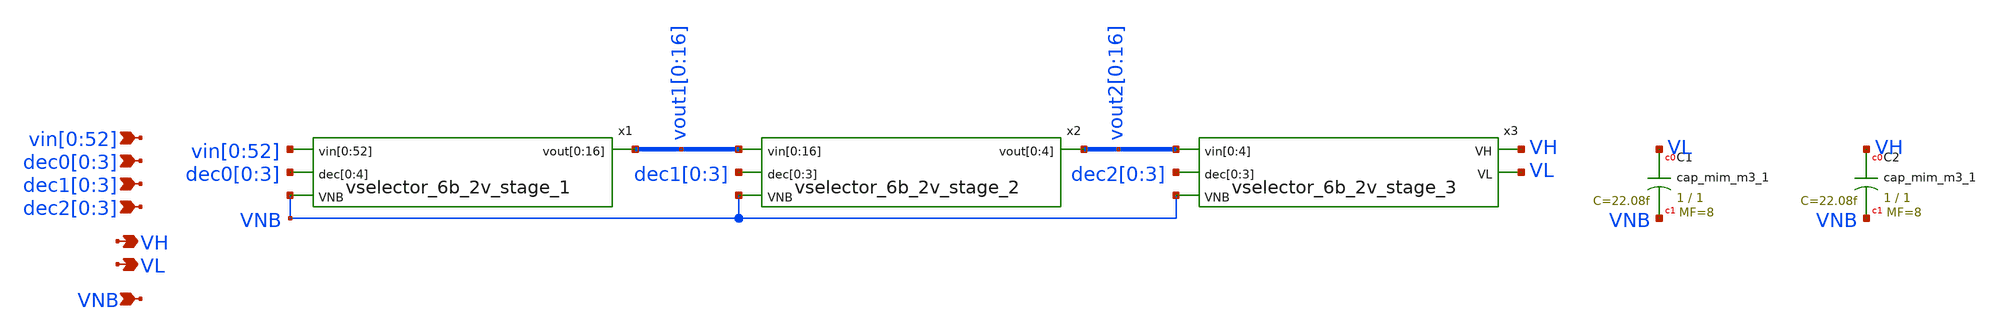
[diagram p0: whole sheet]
** sch_path: xschem/vselector_6b_2v.sch
**.subckt vselector_6b_2v
*+ vin[0],vin[1],vin[2],vin[3],vin[4],vin[5],vin[6],vin[7],vin[8],vin[9],vin[10],vin[11],vin[12],vin[13],vin[14],vin[15],vin[16],vin[17],vin[18],vin[19],vin[20],vin[21],vin[22],vin[23],vin[24],vin[25],vin[26],vin[27],vin[28],vin[29],vin[30],vin[31],vin[32],vin[33],vin[34],vin[35],vin[36],vin[37],vin[38],vin[39],vin[40],vin[41],vin[42],vin[43],vin[44],vin[45],vin[46],vin[47],vin[48],vin[49],vin[50],vin[51],vin[52] VH VNB dec0[0],dec0[1],dec0[2],dec0[3] VL dec1[0],dec1[1],dec1[2],dec1[3]
*+ dec2[0],dec2[1],dec2[2],dec2[3]
*.ipin
*+ vin[0],vin[1],vin[2],vin[3],vin[4],vin[5],vin[6],vin[7],vin[8],vin[9],vin[10],vin[11],vin[12],vin[13],vin[14],vin[15],vin[16],vin[17],vin[18],vin[19],vin[20],vin[21],vin[22],vin[23],vin[24],vin[25],vin[26],vin[27],vin[28],vin[29],vin[30],vin[31],vin[32],vin[33],vin[34],vin[35],vin[36],vin[37],vin[38],vin[39],vin[40],vin[41],vin[42],vin[43],vin[44],vin[45],vin[46],vin[47],vin[48],vin[49],vin[50],vin[51],vin[52]
*.opin VH
*.ipin VNB
*.ipin dec0[0],dec0[1],dec0[2],dec0[3]
*.opin VL
*.ipin dec1[0],dec1[1],dec1[2],dec1[3]
*.ipin dec2[0],dec2[1],dec2[2],dec2[3]
x1 vin[0] vin[1] vin[2] vin[3] vin[4] vin[5] vin[6] vin[7] vin[8] vin[9] vin[10] vin[11] vin[12]
+ vin[13] vin[14] vin[15] vin[16] vin[17] vin[18] vin[19] vin[20] vin[21] vin[22] vin[23] vin[24] vin[25]
+ vin[26] vin[27] vin[28] vin[29] vin[30] vin[31] vin[32] vin[33] vin[34] vin[35] vin[36] vin[37] vin[38]
+ vin[39] vin[40] vin[41] vin[42] vin[43] vin[44] vin[45] vin[46] vin[47] vin[48] vin[49] vin[50] vin[51]
+ vin[52] dec0[0] dec0[1] dec0[2] dec0[3] dec0[0] vout1[0] vout1[1] vout1[2] vout1[3] vout1[4] vout1[5]
+ vout1[6] vout1[7] vout1[8] vout1[9] vout1[10] vout1[11] vout1[12] vout1[13] vout1[14] vout1[15] vout1[16]
+ VNB vselector_6b_2v_stage_1
x2 vout1[0] vout1[1] vout1[2] vout1[3] vout1[4] vout1[5] vout1[6] vout1[7] vout1[8] vout1[9]
+ vout1[10] vout1[11] vout1[12] vout1[13] vout1[14] vout1[15] vout1[16] dec1[0] dec1[1] dec1[2] dec1[3]
+ vout2[0] vout2[1] vout2[2] vout2[3] vout2[4] VNB vselector_6b_2v_stage_2
x3 vout2[0] vout2[1] vout2[2] vout2[3] vout2[4] dec2[0] dec2[1] dec2[2] dec2[3] VH VL VNB
+ vselector_6b_2v_stage_3
XC1 VL VNB sky130_fd_pr__cap_mim_m3_1 W=1 L=1 MF=8 m=8
XC2 VH VNB sky130_fd_pr__cap_mim_m3_1 W=1 L=1 MF=8 m=8
**.ends

* expanding   symbol:  vselector_6b_2v_stage_1.sym # of pins=4
** sym_path: xschem/vselector_6b_2v_stage_1.sym
** sch_path: xschem/vselector_6b_2v_stage_1.sch
.subckt vselector_6b_2v_stage_1 vin[0] vin[1] vin[2] vin[3] vin[4] vin[5] vin[6] vin[7] vin[8]
+ vin[9] vin[10] vin[11] vin[12] vin[13] vin[14] vin[15] vin[16] vin[17] vin[18] vin[19] vin[20] vin[21]
+ vin[22] vin[23] vin[24] vin[25] vin[26] vin[27] vin[28] vin[29] vin[30] vin[31] vin[32] vin[33] vin[34]
+ vin[35] vin[36] vin[37] vin[38] vin[39] vin[40] vin[41] vin[42] vin[43] vin[44] vin[45] vin[46] vin[47]
+ vin[48] vin[49] vin[50] vin[51] vin[52] dec[0] dec[1] dec[2] dec[3] dec[4] vout[0] vout[1] vout[2] vout[3]
+ vout[4] vout[5] vout[6] vout[7] vout[8] vout[9] vout[10] vout[11] vout[12] vout[13] vout[14] vout[15]
+ vout[16] VNB
*.ipin
*+ vin[0],vin[1],vin[2],vin[3],vin[4],vin[5],vin[6],vin[7],vin[8],vin[9],vin[10],vin[11],vin[12],vin[13],vin[14],vin[15],vin[16],vin[17],vin[18],vin[19],vin[20],vin[21],vin[22],vin[23],vin[24],vin[25],vin[26],vin[27],vin[28],vin[29],vin[30],vin[31],vin[32],vin[33],vin[34],vin[35],vin[36],vin[37],vin[38],vin[39],vin[40],vin[41],vin[42],vin[43],vin[44],vin[45],vin[46],vin[47],vin[48],vin[49],vin[50],vin[51],vin[52]
*.opin
*+ vout[0],vout[1],vout[2],vout[3],vout[4],vout[5],vout[6],vout[7],vout[8],vout[9],vout[10],vout[11],vout[12],vout[13],vout[14],vout[15],vout[16]
*.ipin VNB
*.ipin dec[0],dec[1],dec[2],dec[3],dec[4]
x1 vin[0] vin[1] vin[2] vin[3] vin[4] vin[5] vin[6] vin[7] vin[8] vin[9] vin[10] vin[11] vin[12]
+ vin[13] vin[14] vin[15] vin[16] dec[0] vout[0] vout[1] vout[2] vout[3] vout[4] vout[5] vout[6] vout[7]
+ vout[8] vout[9] vout[10] vout[11] vout[12] vout[13] vout[14] vout[15] vout[16] VNB vselector_16b
x2 vin[16] vin[17] vin[18] vin[19] vin[20] vin[21] vin[22] vin[23] vin[24] vin[25] vin[26] vin[27]
+ vin[28] vin[29] vin[30] vin[31] vin[32] dec[1] vout[0] vout[1] vout[2] vout[3] vout[4] vout[5] vout[6]
+ vout[7] vout[8] vout[9] vout[10] vout[11] vout[12] vout[13] vout[14] vout[15] vout[16] VNB vselector_16b
x3 vin[32] vin[33] vin[34] vin[35] vin[36] vin[37] vin[38] vin[39] vin[40] vin[41] vin[42] vin[43]
+ vin[44] vin[45] vin[46] vin[47] vin[48] dec[2] vout[0] vout[1] vout[2] vout[3] vout[4] vout[5] vout[6]
+ vout[7] vout[8] vout[9] vout[10] vout[11] vout[12] vout[13] vout[14] vout[15] vout[16] VNB vselector_16b
x4 vin[48] vin[49] vin[50] vin[51] vin[52] dec[3] vout[0] vout[1] vout[2] vout[3] vout[4] VNB
+ vselector_4b
.ends


* expanding   symbol:  vselector_6b_2v_stage_2.sym # of pins=4
** sym_path: xschem/vselector_6b_2v_stage_2.sym
** sch_path: xschem/vselector_6b_2v_stage_2.sch
.subckt vselector_6b_2v_stage_2 vin[0] vin[1] vin[2] vin[3] vin[4] vin[5] vin[6] vin[7] vin[8]
+ vin[9] vin[10] vin[11] vin[12] vin[13] vin[14] vin[15] vin[16] dec[0] dec[1] dec[2] dec[3] vout[0] vout[1]
+ vout[2] vout[3] vout[4] VNB
*.ipin
*+ vin[0],vin[1],vin[2],vin[3],vin[4],vin[5],vin[6],vin[7],vin[8],vin[9],vin[10],vin[11],vin[12],vin[13],vin[14],vin[15],vin[16]
*.opin vout[0],vout[1],vout[2],vout[3],vout[4]
*.ipin VNB
*.ipin dec[0],dec[1],dec[2],dec[3]
x1 vin[0] vin[1] vin[2] vin[3] vin[4] dec[0] vout[0] vout[1] vout[2] vout[3] vout[4] VNB
+ vselector_4b
x2 vin[4] vin[5] vin[6] vin[7] vin[8] dec[1] vout[0] vout[1] vout[2] vout[3] vout[4] VNB
+ vselector_4b
x3 vin[8] vin[9] vin[10] vin[11] vin[12] dec[2] vout[0] vout[1] vout[2] vout[3] vout[4] VNB
+ vselector_4b
x4 vin[12] vin[13] vin[14] vin[15] vin[16] dec[3] vout[0] vout[1] vout[2] vout[3] vout[4] VNB
+ vselector_4b
.ends


* expanding   symbol:  vselector_6b_2v_stage_3.sym # of pins=5
** sym_path: xschem/vselector_6b_2v_stage_3.sym
** sch_path: xschem/vselector_6b_2v_stage_3.sch
.subckt vselector_6b_2v_stage_3 vin[0] vin[1] vin[2] vin[3] vin[4] dec[0] dec[1] dec[2] dec[3] VH VL
+ VNB
*.ipin vin[0],vin[1],vin[2],vin[3],vin[4]
*.opin VH
*.ipin VNB
*.ipin dec[0],dec[1],dec[2],dec[3]
*.opin VL
x1 vin[0] vin[1] dec[0] VH VL VNB vselector_1b
x2 vin[1] vin[2] dec[1] VH VL VNB vselector_1b
x3 vin[2] vin[3] dec[2] VH VL VNB vselector_1b
x4 vin[3] vin[4] dec[3] VH VL VNB vselector_1b
.ends


* expanding   symbol:  vselector_16b.sym # of pins=4
** sym_path: xschem/vselector_16b.sym
** sch_path: xschem/vselector_16b.sch
.subckt vselector_16b vin[0] vin[1] vin[2] vin[3] vin[4] vin[5] vin[6] vin[7] vin[8] vin[9] vin[10]
+ vin[11] vin[12] vin[13] vin[14] vin[15] vin[16] DIN vout[0] vout[1] vout[2] vout[3] vout[4] vout[5] vout[6]
+ vout[7] vout[8] vout[9] vout[10] vout[11] vout[12] vout[13] vout[14] vout[15] vout[16] VNB
*.ipin
*+ vin[0],vin[1],vin[2],vin[3],vin[4],vin[5],vin[6],vin[7],vin[8],vin[9],vin[10],vin[11],vin[12],vin[13],vin[14],vin[15],vin[16]
*.opin
*+ vout[0],vout[1],vout[2],vout[3],vout[4],vout[5],vout[6],vout[7],vout[8],vout[9],vout[10],vout[11],vout[12],vout[13],vout[14],vout[15],vout[16]
*.ipin VNB
*.ipin DIN
XM1 vout[0] DIN vin[0] VNB sky130_fd_pr__nfet_g5v0d10v5 L=l W=wn nf=1 ad='int((nf+1)/2) * W/nf * 0.29'
+ as='int((nf+2)/2) * W/nf * 0.29' pd='2*int((nf+1)/2) * (W/nf + 0.29)' ps='2*int((nf+2)/2) * (W/nf + 0.29)'
+ nrd='0.29 / W' nrs='0.29 / W' sa=0 sb=0 sd=0 mult=1 m=1
XM2 vout[1] DIN vin[1] VNB sky130_fd_pr__nfet_g5v0d10v5 L=l W=wn nf=1 ad='int((nf+1)/2) * W/nf * 0.29'
+ as='int((nf+2)/2) * W/nf * 0.29' pd='2*int((nf+1)/2) * (W/nf + 0.29)' ps='2*int((nf+2)/2) * (W/nf + 0.29)'
+ nrd='0.29 / W' nrs='0.29 / W' sa=0 sb=0 sd=0 mult=1 m=1
XM3 vout[2] DIN vin[2] VNB sky130_fd_pr__nfet_g5v0d10v5 L=l W=wn nf=1 ad='int((nf+1)/2) * W/nf * 0.29'
+ as='int((nf+2)/2) * W/nf * 0.29' pd='2*int((nf+1)/2) * (W/nf + 0.29)' ps='2*int((nf+2)/2) * (W/nf + 0.29)'
+ nrd='0.29 / W' nrs='0.29 / W' sa=0 sb=0 sd=0 mult=1 m=1
XM4 vout[3] DIN vin[3] VNB sky130_fd_pr__nfet_g5v0d10v5 L=l W=wn nf=1 ad='int((nf+1)/2) * W/nf * 0.29'
+ as='int((nf+2)/2) * W/nf * 0.29' pd='2*int((nf+1)/2) * (W/nf + 0.29)' ps='2*int((nf+2)/2) * (W/nf + 0.29)'
+ nrd='0.29 / W' nrs='0.29 / W' sa=0 sb=0 sd=0 mult=1 m=1
XM5 vout[4] DIN vin[4] VNB sky130_fd_pr__nfet_g5v0d10v5 L=l W=wn nf=1 ad='int((nf+1)/2) * W/nf * 0.29'
+ as='int((nf+2)/2) * W/nf * 0.29' pd='2*int((nf+1)/2) * (W/nf + 0.29)' ps='2*int((nf+2)/2) * (W/nf + 0.29)'
+ nrd='0.29 / W' nrs='0.29 / W' sa=0 sb=0 sd=0 mult=1 m=1
XM6 vout[5] DIN vin[5] VNB sky130_fd_pr__nfet_g5v0d10v5 L=l W=wn nf=1 ad='int((nf+1)/2) * W/nf * 0.29'
+ as='int((nf+2)/2) * W/nf * 0.29' pd='2*int((nf+1)/2) * (W/nf + 0.29)' ps='2*int((nf+2)/2) * (W/nf + 0.29)'
+ nrd='0.29 / W' nrs='0.29 / W' sa=0 sb=0 sd=0 mult=1 m=1
XM7 vout[6] DIN vin[6] VNB sky130_fd_pr__nfet_g5v0d10v5 L=l W=wn nf=1 ad='int((nf+1)/2) * W/nf * 0.29'
+ as='int((nf+2)/2) * W/nf * 0.29' pd='2*int((nf+1)/2) * (W/nf + 0.29)' ps='2*int((nf+2)/2) * (W/nf + 0.29)'
+ nrd='0.29 / W' nrs='0.29 / W' sa=0 sb=0 sd=0 mult=1 m=1
XM8 vout[7] DIN vin[7] VNB sky130_fd_pr__nfet_g5v0d10v5 L=l W=wn nf=1 ad='int((nf+1)/2) * W/nf * 0.29'
+ as='int((nf+2)/2) * W/nf * 0.29' pd='2*int((nf+1)/2) * (W/nf + 0.29)' ps='2*int((nf+2)/2) * (W/nf + 0.29)'
+ nrd='0.29 / W' nrs='0.29 / W' sa=0 sb=0 sd=0 mult=1 m=1
XM9 vout[8] DIN vin[8] VNB sky130_fd_pr__nfet_g5v0d10v5 L=l W=wn nf=1 ad='int((nf+1)/2) * W/nf * 0.29'
+ as='int((nf+2)/2) * W/nf * 0.29' pd='2*int((nf+1)/2) * (W/nf + 0.29)' ps='2*int((nf+2)/2) * (W/nf + 0.29)'
+ nrd='0.29 / W' nrs='0.29 / W' sa=0 sb=0 sd=0 mult=1 m=1
XM10 vout[9] DIN vin[9] VNB sky130_fd_pr__nfet_g5v0d10v5 L=l W=wn nf=1 ad='int((nf+1)/2) * W/nf * 0.29'
+ as='int((nf+2)/2) * W/nf * 0.29' pd='2*int((nf+1)/2) * (W/nf + 0.29)' ps='2*int((nf+2)/2) * (W/nf + 0.29)'
+ nrd='0.29 / W' nrs='0.29 / W' sa=0 sb=0 sd=0 mult=1 m=1
XM11 vout[10] DIN vin[10] VNB sky130_fd_pr__nfet_g5v0d10v5 L=l W=wn nf=1 ad='int((nf+1)/2) * W/nf * 0.29'
+ as='int((nf+2)/2) * W/nf * 0.29' pd='2*int((nf+1)/2) * (W/nf + 0.29)' ps='2*int((nf+2)/2) * (W/nf + 0.29)'
+ nrd='0.29 / W' nrs='0.29 / W' sa=0 sb=0 sd=0 mult=1 m=1
XM12 vout[11] DIN vin[11] VNB sky130_fd_pr__nfet_g5v0d10v5 L=l W=wn nf=1 ad='int((nf+1)/2) * W/nf * 0.29'
+ as='int((nf+2)/2) * W/nf * 0.29' pd='2*int((nf+1)/2) * (W/nf + 0.29)' ps='2*int((nf+2)/2) * (W/nf + 0.29)'
+ nrd='0.29 / W' nrs='0.29 / W' sa=0 sb=0 sd=0 mult=1 m=1
XM13 vout[12] DIN vin[12] VNB sky130_fd_pr__nfet_g5v0d10v5 L=l W=wn nf=1 ad='int((nf+1)/2) * W/nf * 0.29'
+ as='int((nf+2)/2) * W/nf * 0.29' pd='2*int((nf+1)/2) * (W/nf + 0.29)' ps='2*int((nf+2)/2) * (W/nf + 0.29)'
+ nrd='0.29 / W' nrs='0.29 / W' sa=0 sb=0 sd=0 mult=1 m=1
XM14 vout[13] DIN vin[13] VNB sky130_fd_pr__nfet_g5v0d10v5 L=l W=wn nf=1 ad='int((nf+1)/2) * W/nf * 0.29'
+ as='int((nf+2)/2) * W/nf * 0.29' pd='2*int((nf+1)/2) * (W/nf + 0.29)' ps='2*int((nf+2)/2) * (W/nf + 0.29)'
+ nrd='0.29 / W' nrs='0.29 / W' sa=0 sb=0 sd=0 mult=1 m=1
XM15 vout[14] DIN vin[14] VNB sky130_fd_pr__nfet_g5v0d10v5 L=l W=wn nf=1 ad='int((nf+1)/2) * W/nf * 0.29'
+ as='int((nf+2)/2) * W/nf * 0.29' pd='2*int((nf+1)/2) * (W/nf + 0.29)' ps='2*int((nf+2)/2) * (W/nf + 0.29)'
+ nrd='0.29 / W' nrs='0.29 / W' sa=0 sb=0 sd=0 mult=1 m=1
XM16 vout[15] DIN vin[15] VNB sky130_fd_pr__nfet_g5v0d10v5 L=l W=wn nf=1 ad='int((nf+1)/2) * W/nf * 0.29'
+ as='int((nf+2)/2) * W/nf * 0.29' pd='2*int((nf+1)/2) * (W/nf + 0.29)' ps='2*int((nf+2)/2) * (W/nf + 0.29)'
+ nrd='0.29 / W' nrs='0.29 / W' sa=0 sb=0 sd=0 mult=1 m=1
XM17 vout[16] DIN vin[16] VNB sky130_fd_pr__nfet_g5v0d10v5 L=l W=wn nf=1 ad='int((nf+1)/2) * W/nf * 0.29'
+ as='int((nf+2)/2) * W/nf * 0.29' pd='2*int((nf+1)/2) * (W/nf + 0.29)' ps='2*int((nf+2)/2) * (W/nf + 0.29)'
+ nrd='0.29 / W' nrs='0.29 / W' sa=0 sb=0 sd=0 mult=1 m=1
.ends


* expanding   symbol:  vselector_4b.sym # of pins=4
** sym_path: xschem/vselector_4b.sym
** sch_path: xschem/vselector_4b.sch
.subckt vselector_4b vin[0] vin[1] vin[2] vin[3] vin[4] DIN vout[0] vout[1] vout[2] vout[3] vout[4]
+ VNB
*.ipin vin[0],vin[1],vin[2],vin[3],vin[4]
*.opin vout[0],vout[1],vout[2],vout[3],vout[4]
*.ipin VNB
*.ipin DIN
XM1 vout[0] DIN vin[0] VNB sky130_fd_pr__nfet_g5v0d10v5 L=l W=wn nf=1 ad='int((nf+1)/2) * W/nf * 0.29'
+ as='int((nf+2)/2) * W/nf * 0.29' pd='2*int((nf+1)/2) * (W/nf + 0.29)' ps='2*int((nf+2)/2) * (W/nf + 0.29)'
+ nrd='0.29 / W' nrs='0.29 / W' sa=0 sb=0 sd=0 mult=1 m=1
XM2 vout[1] DIN vin[1] VNB sky130_fd_pr__nfet_g5v0d10v5 L=l W=wn nf=1 ad='int((nf+1)/2) * W/nf * 0.29'
+ as='int((nf+2)/2) * W/nf * 0.29' pd='2*int((nf+1)/2) * (W/nf + 0.29)' ps='2*int((nf+2)/2) * (W/nf + 0.29)'
+ nrd='0.29 / W' nrs='0.29 / W' sa=0 sb=0 sd=0 mult=1 m=1
XM3 vout[2] DIN vin[2] VNB sky130_fd_pr__nfet_g5v0d10v5 L=l W=wn nf=1 ad='int((nf+1)/2) * W/nf * 0.29'
+ as='int((nf+2)/2) * W/nf * 0.29' pd='2*int((nf+1)/2) * (W/nf + 0.29)' ps='2*int((nf+2)/2) * (W/nf + 0.29)'
+ nrd='0.29 / W' nrs='0.29 / W' sa=0 sb=0 sd=0 mult=1 m=1
XM4 vout[3] DIN vin[3] VNB sky130_fd_pr__nfet_g5v0d10v5 L=l W=wn nf=1 ad='int((nf+1)/2) * W/nf * 0.29'
+ as='int((nf+2)/2) * W/nf * 0.29' pd='2*int((nf+1)/2) * (W/nf + 0.29)' ps='2*int((nf+2)/2) * (W/nf + 0.29)'
+ nrd='0.29 / W' nrs='0.29 / W' sa=0 sb=0 sd=0 mult=1 m=1
XM5 vout[4] DIN vin[4] VNB sky130_fd_pr__nfet_g5v0d10v5 L=l W=wn nf=1 ad='int((nf+1)/2) * W/nf * 0.29'
+ as='int((nf+2)/2) * W/nf * 0.29' pd='2*int((nf+1)/2) * (W/nf + 0.29)' ps='2*int((nf+2)/2) * (W/nf + 0.29)'
+ nrd='0.29 / W' nrs='0.29 / W' sa=0 sb=0 sd=0 mult=1 m=1
.ends


* expanding   symbol:  vselector_1b.sym # of pins=5
** sym_path: xschem/vselector_1b.sym
** sch_path: xschem/vselector_1b.sch
.subckt vselector_1b vin[0] vin[1] DIN VH VL VNB
*.ipin vin[0],vin[1]
*.opin VL
*.ipin VNB
*.ipin DIN
*.opin VH
.param wp=0.42 wn=0.42 l=0.5

XM1 VL DIN vin[0] VNB sky130_fd_pr__nfet_g5v0d10v5 L=l W=wn nf=1 ad='int((nf+1)/2) * W/nf * 0.29' as='int((nf+2)/2) * W/nf * 0.29'
+ pd='2*int((nf+1)/2) * (W/nf + 0.29)' ps='2*int((nf+2)/2) * (W/nf + 0.29)' nrd='0.29 / W' nrs='0.29 / W'
+ sa=0 sb=0 sd=0 mult=1 m=1
XM2 VH DIN vin[1] VNB sky130_fd_pr__nfet_g5v0d10v5 L=l W=wn nf=1 ad='int((nf+1)/2) * W/nf * 0.29' as='int((nf+2)/2) * W/nf * 0.29'
+ pd='2*int((nf+1)/2) * (W/nf + 0.29)' ps='2*int((nf+2)/2) * (W/nf + 0.29)' nrd='0.29 / W' nrs='0.29 / W'
+ sa=0 sb=0 sd=0 mult=1 m=1
.ends

.end
